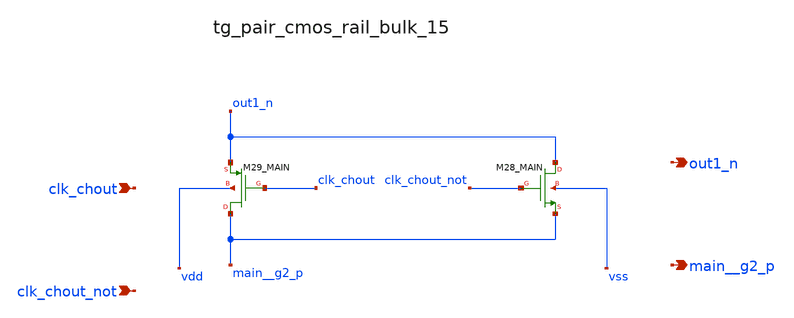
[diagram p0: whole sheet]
** sch_path: analog-db/raw/ia_004_fan_chopper_rrl/hier/blocks/tg_pair_cmos_rail_bulk_15.sch
**.subckt tg_pair_cmos_rail_bulk_15 clk_chout clk_chout_not out1_n main__g2_p
*.ipin clk_chout
*.ipin clk_chout_not
*.opin out1_n
*.opin main__g2_p
XM28_MAIN out1_n clk_chout_not main__g2_p vss sg13_lv_nmos w=x_dut_xm28_main_w l=x_dut_xm28_main_l
+ ng=1 m=x_dut_xm28_main_m
XM29_MAIN main__g2_p clk_chout out1_n vdd sg13_lv_pmos w=x_dut_xm29_main_w l=x_dut_xm29_main_l ng=1
+ m=x_dut_xm29_main_m
**.ends
.end
